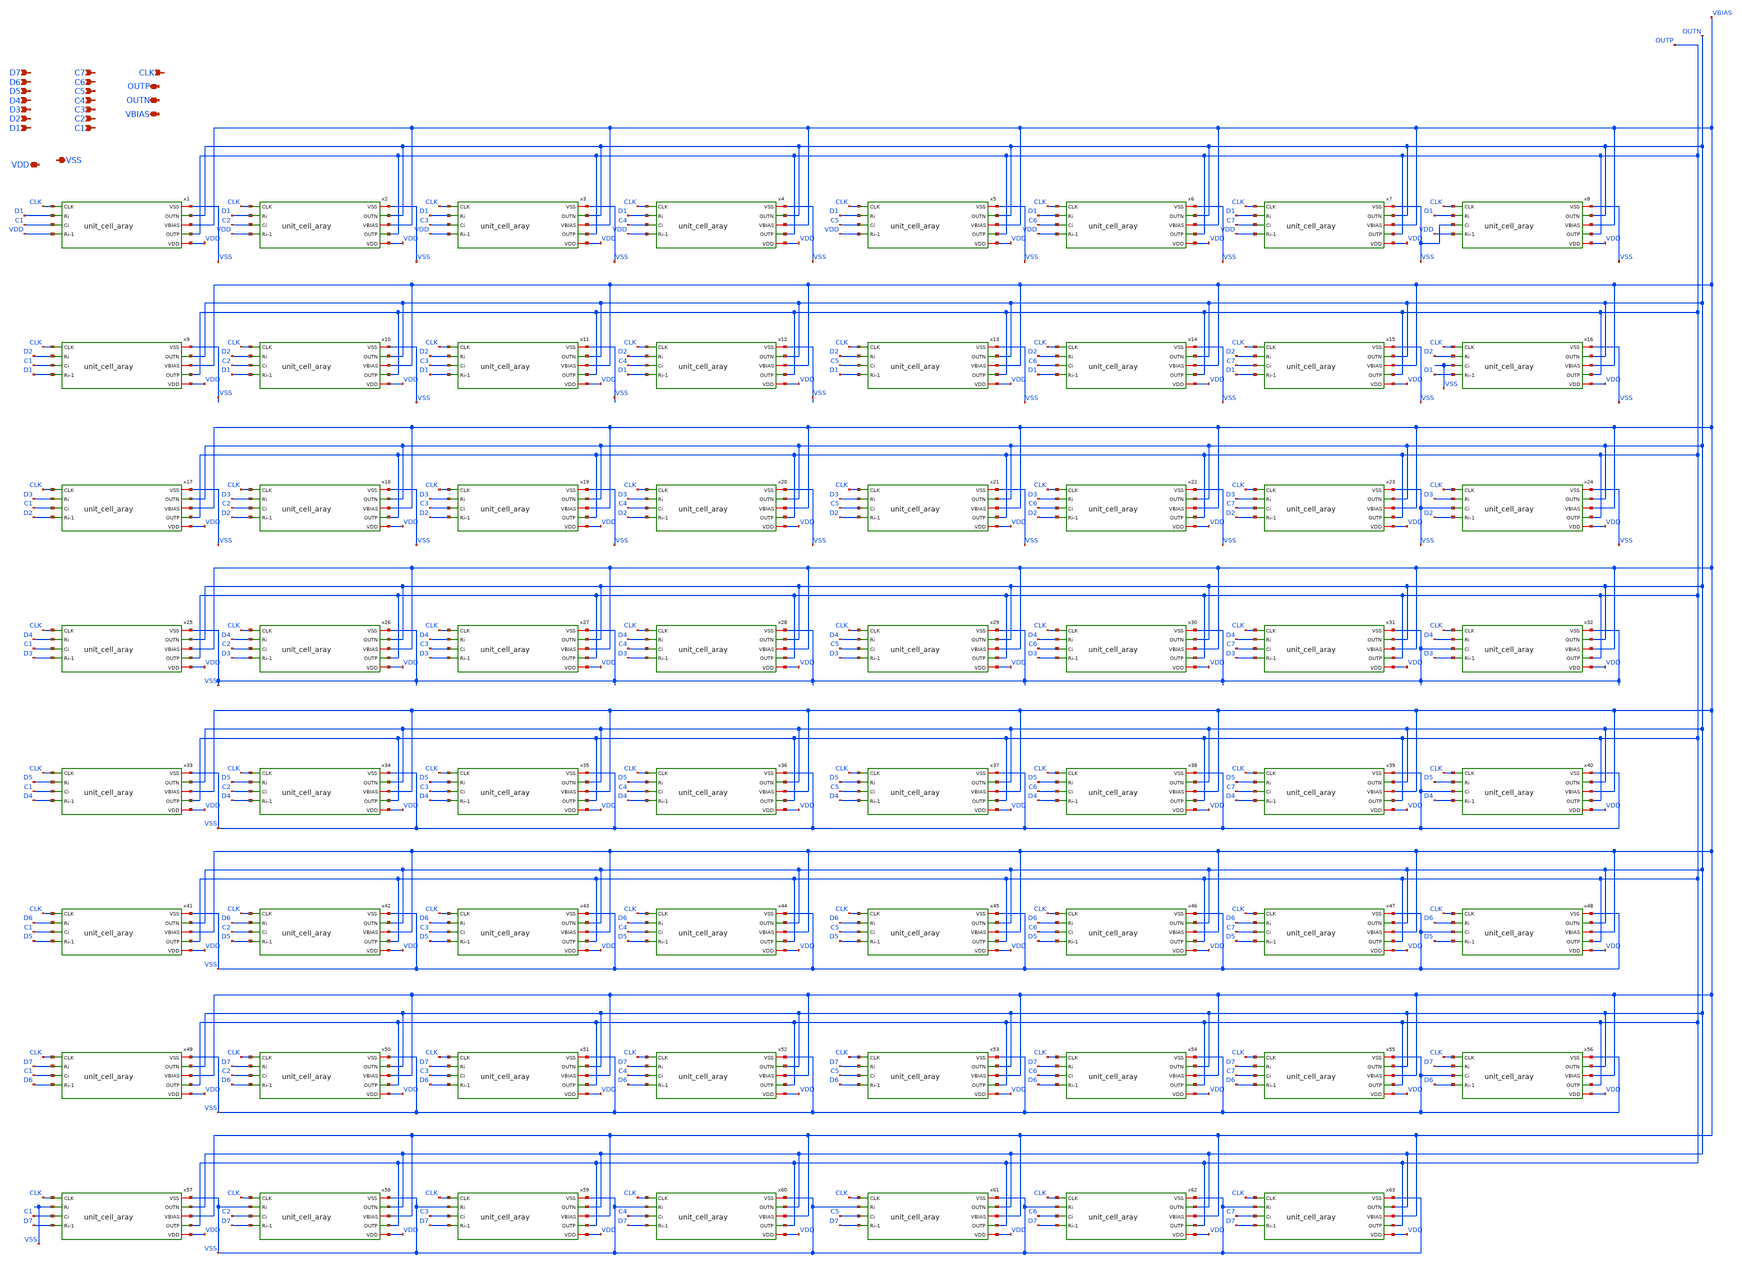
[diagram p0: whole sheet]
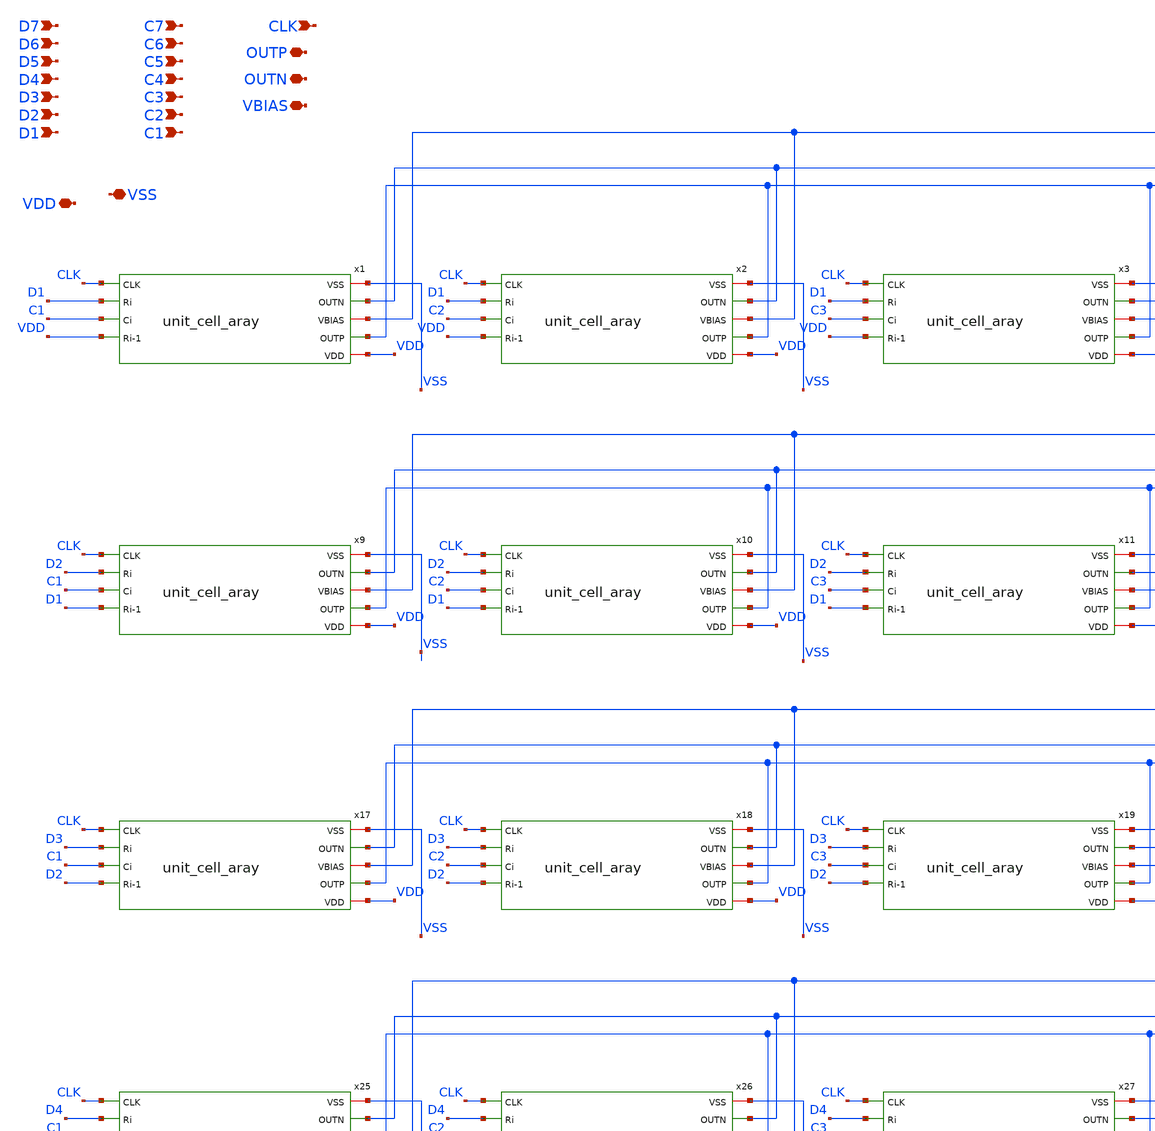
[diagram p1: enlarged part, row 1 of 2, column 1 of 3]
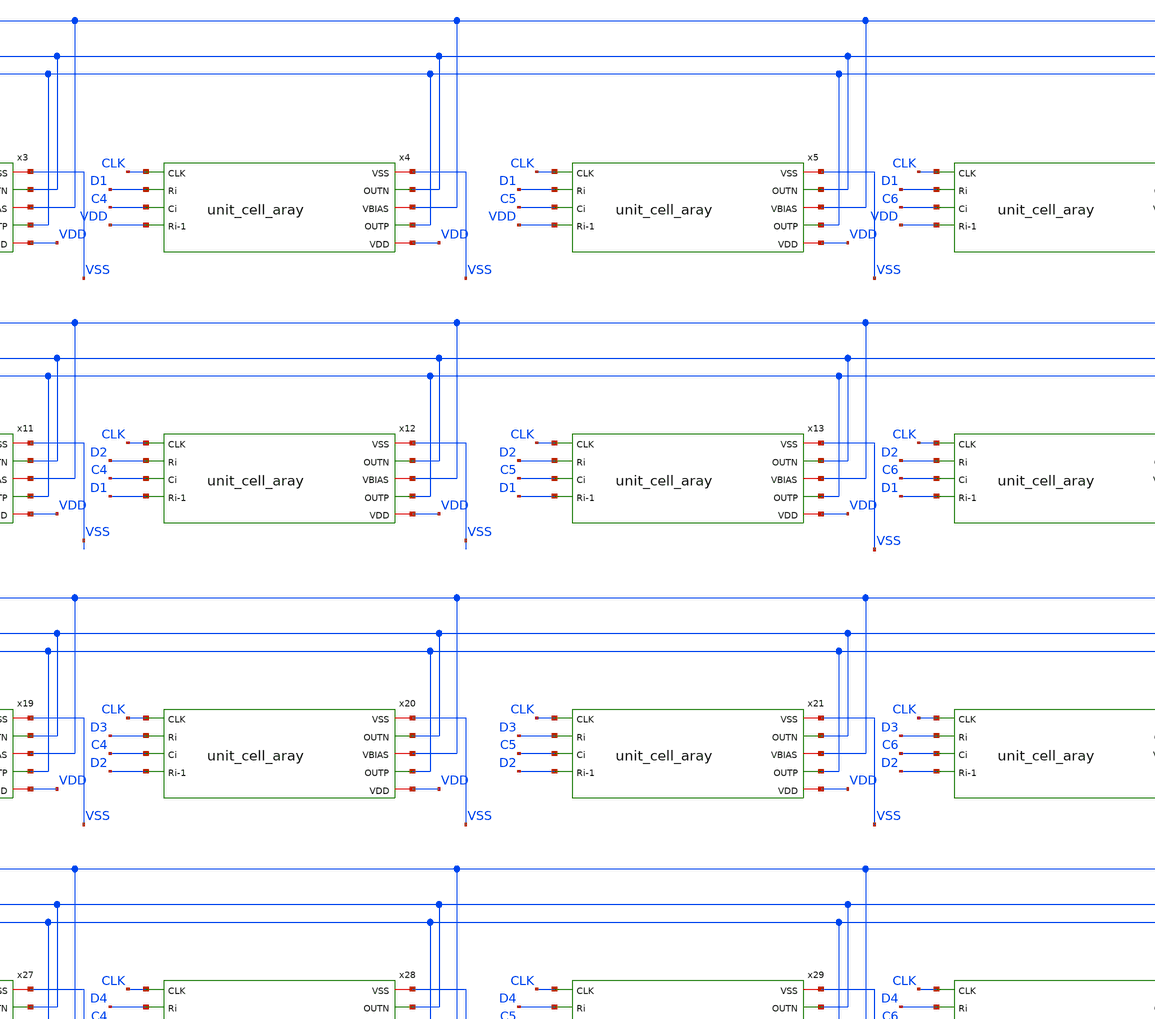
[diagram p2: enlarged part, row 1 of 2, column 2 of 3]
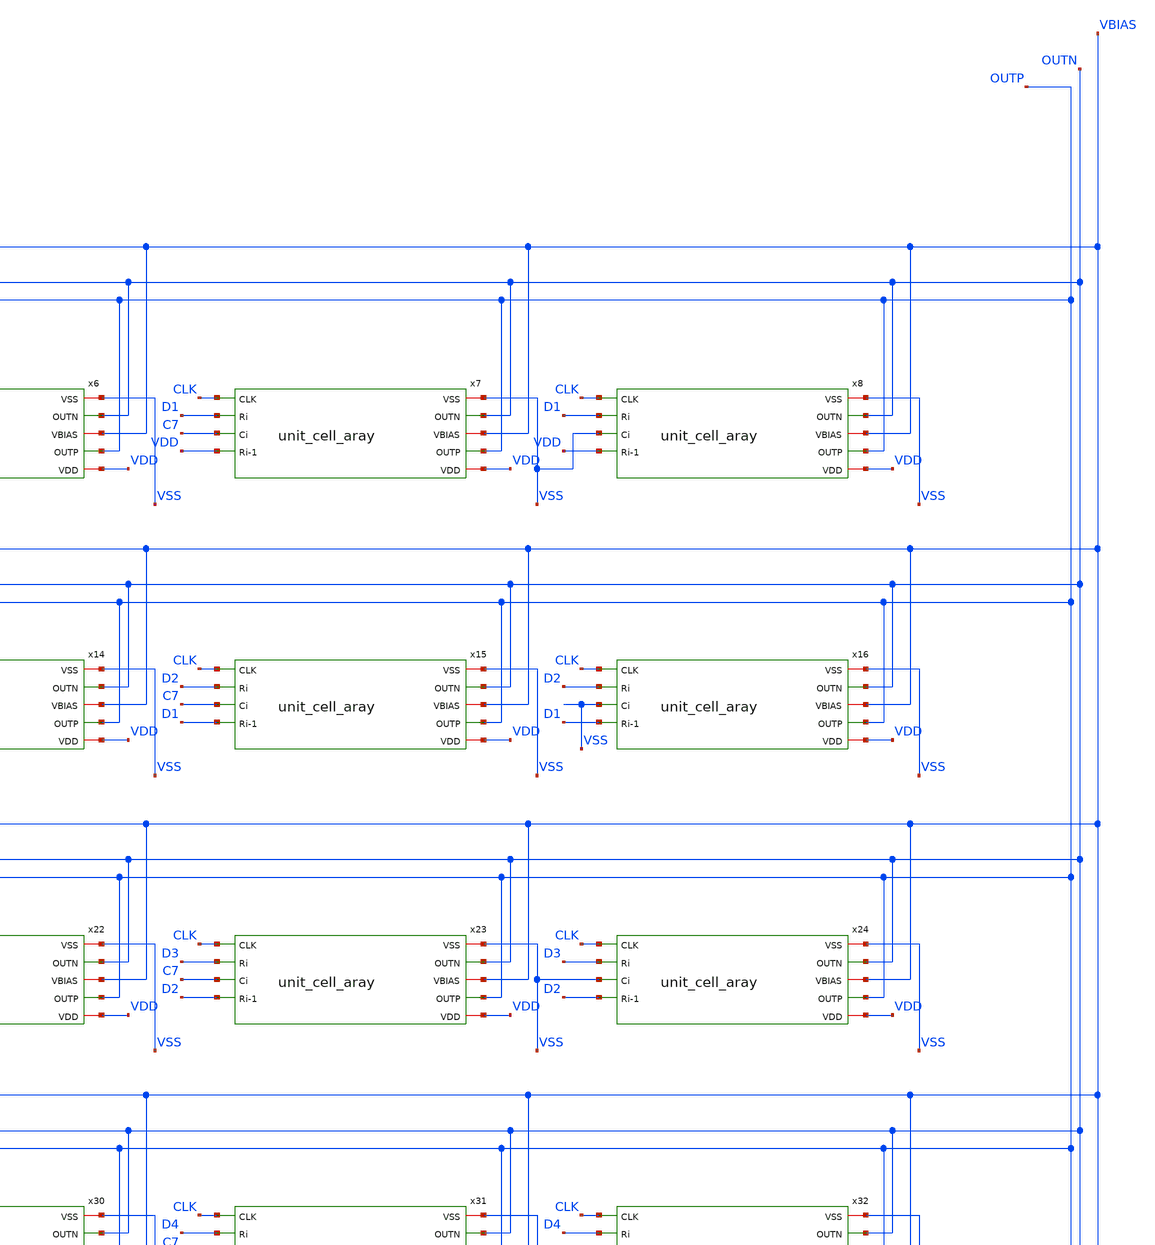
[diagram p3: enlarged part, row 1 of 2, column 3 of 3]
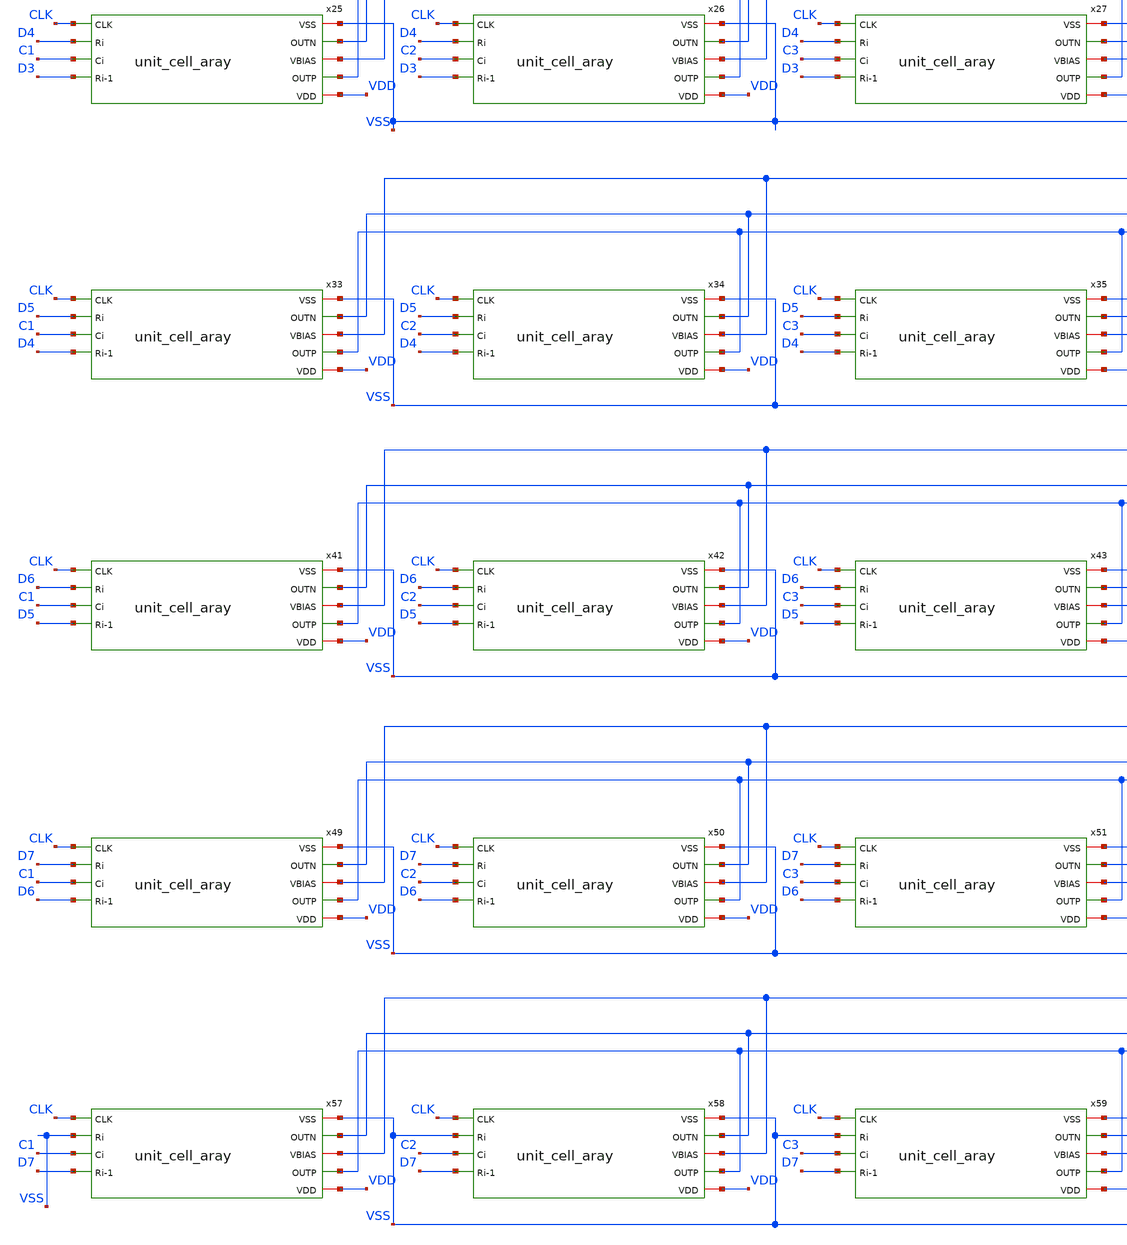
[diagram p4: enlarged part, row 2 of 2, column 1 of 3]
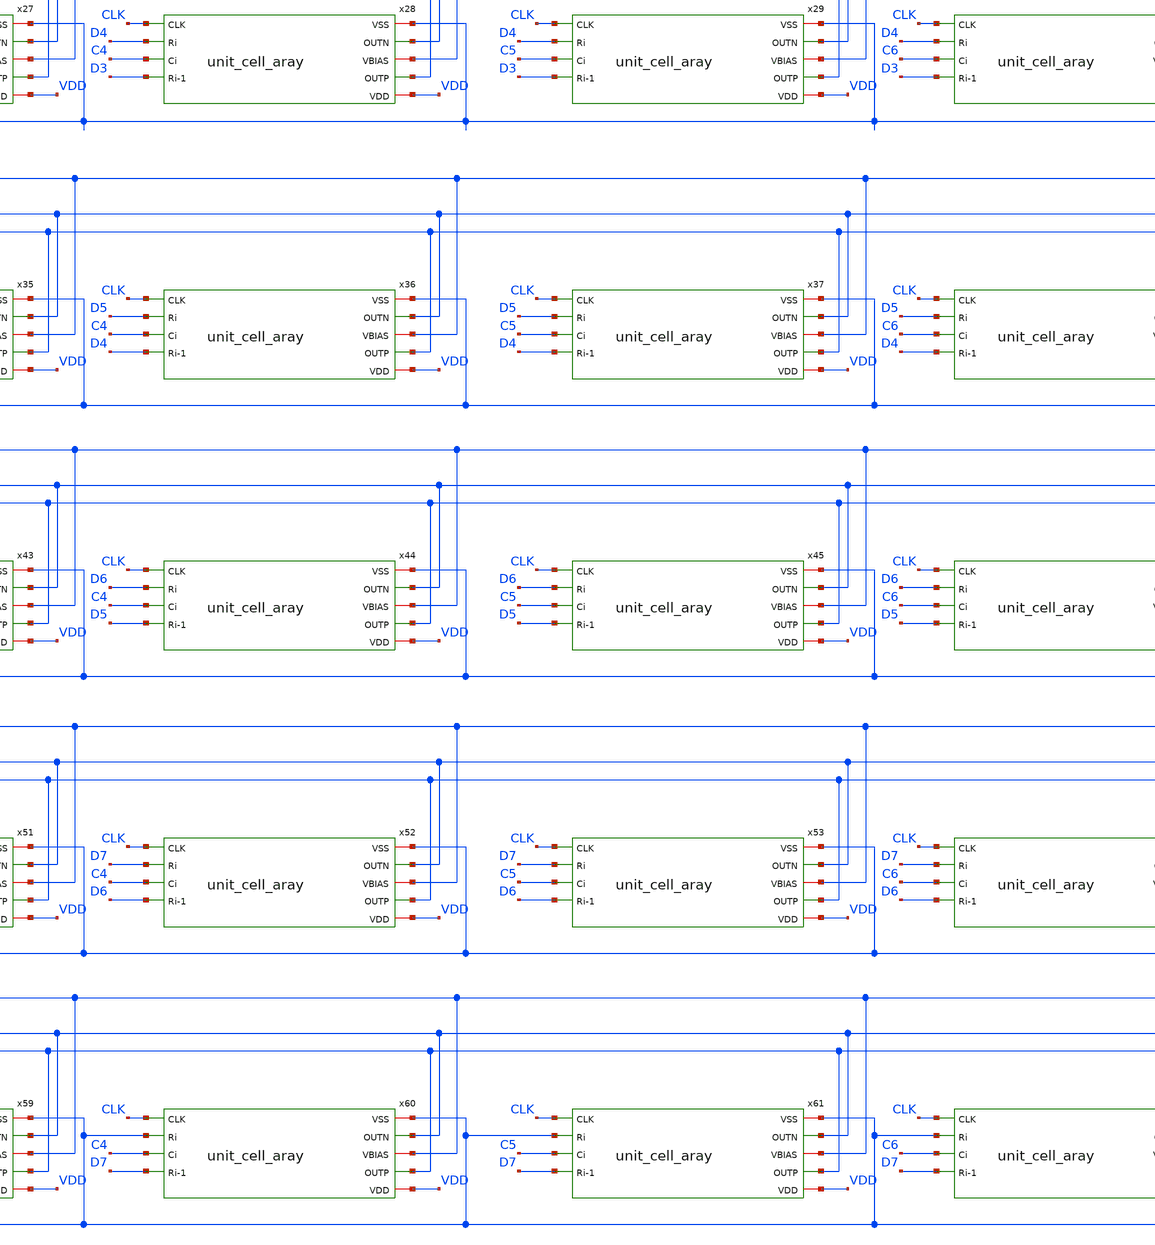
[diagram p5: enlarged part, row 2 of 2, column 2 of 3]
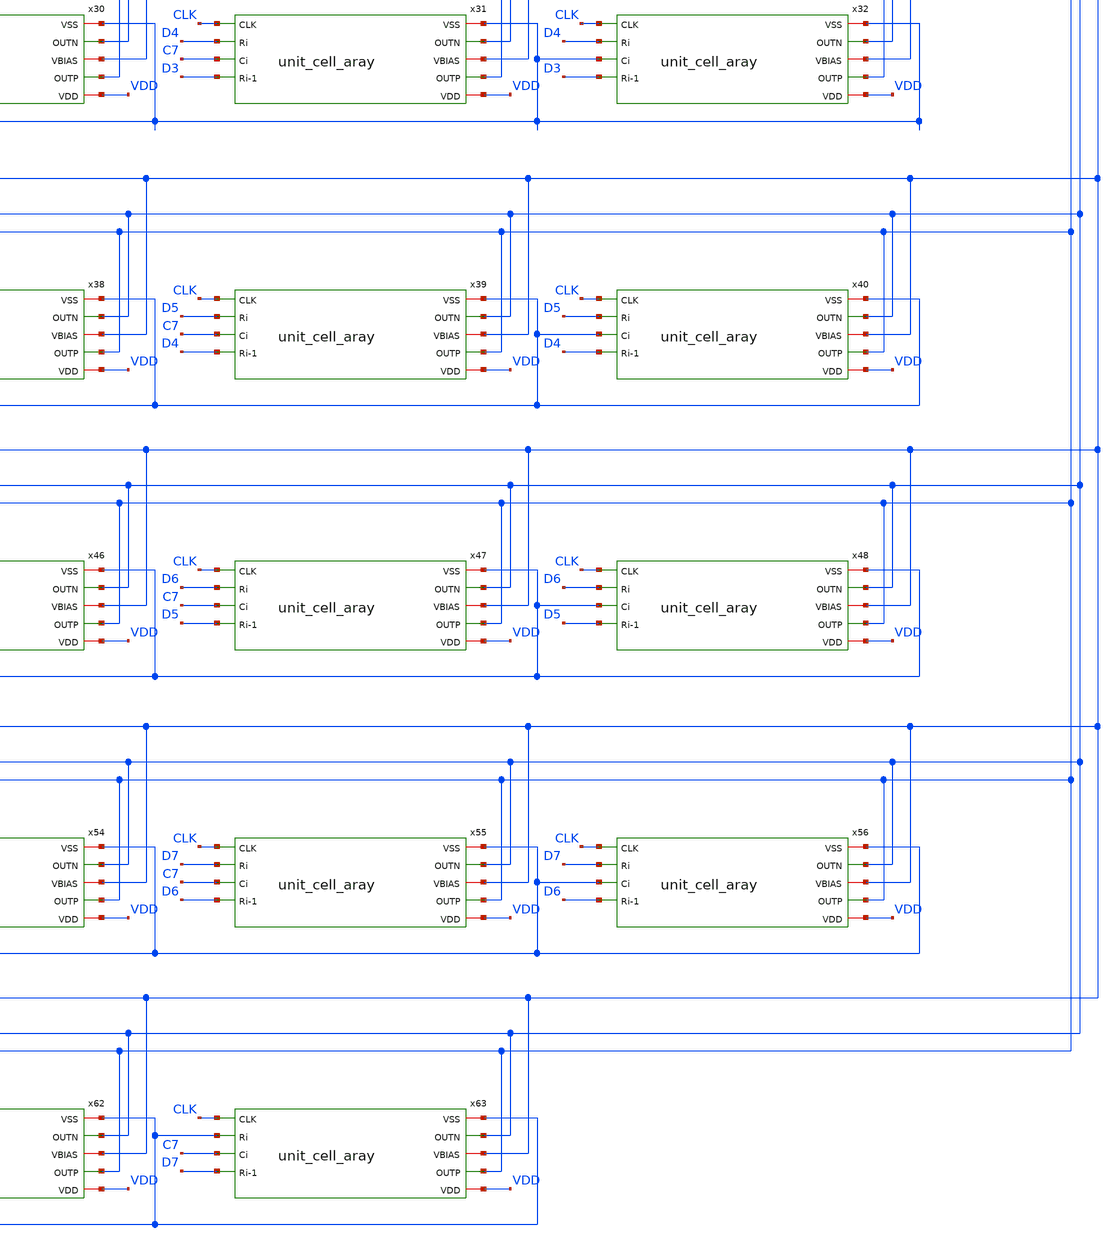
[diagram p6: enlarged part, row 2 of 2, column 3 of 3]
** sch_path: xschem/x6MSB_MATRIX.sch
**.subckt x6MSB_MATRIX D1 D2 D3 D4 D5 D6 D7 C1 C2 C3 C4 C5 C6 C7 CLK OUTP OUTN VBIAS VDD VSS
*.ipin D1
*.ipin D2
*.ipin D3
*.ipin D4
*.ipin D5
*.ipin D6
*.ipin D7
*.ipin C1
*.ipin C2
*.ipin C3
*.ipin C4
*.ipin C5
*.ipin C6
*.ipin C7
*.ipin CLK
*.iopin OUTP
*.iopin OUTN
*.iopin VBIAS
*.iopin VDD
*.iopin VSS
x7 C7 CLK OUTN VBIAS VDD D1 VDD VSS OUTP unit_cell_aray
x8 VSS CLK OUTN VBIAS VDD D1 VDD VSS OUTP unit_cell_aray
x9 C1 CLK OUTN VBIAS D1 D2 VDD VSS OUTP unit_cell_aray
x10 C2 CLK OUTN VBIAS D1 D2 VDD VSS OUTP unit_cell_aray
x11 C3 CLK OUTN VBIAS D1 D2 VDD VSS OUTP unit_cell_aray
x12 C4 CLK OUTN VBIAS D1 D2 VDD VSS OUTP unit_cell_aray
x13 C5 CLK OUTN VBIAS D1 D2 VDD VSS OUTP unit_cell_aray
x14 C6 CLK OUTN VBIAS D1 D2 VDD VSS OUTP unit_cell_aray
x15 C7 CLK OUTN VBIAS D1 D2 VDD VSS OUTP unit_cell_aray
x16 VSS CLK OUTN VBIAS D1 D2 VDD VSS OUTP unit_cell_aray
x17 C1 CLK OUTN VBIAS D2 D3 VDD VSS OUTP unit_cell_aray
x18 C2 CLK OUTN VBIAS D2 D3 VDD VSS OUTP unit_cell_aray
x19 C3 CLK OUTN VBIAS D2 D3 VDD VSS OUTP unit_cell_aray
x20 C4 CLK OUTN VBIAS D2 D3 VDD VSS OUTP unit_cell_aray
x21 C5 CLK OUTN VBIAS D2 D3 VDD VSS OUTP unit_cell_aray
x22 C6 CLK OUTN VBIAS D2 D3 VDD VSS OUTP unit_cell_aray
x23 C7 CLK OUTN VBIAS D2 D3 VDD VSS OUTP unit_cell_aray
x24 VSS CLK OUTN VBIAS D2 D3 VDD VSS OUTP unit_cell_aray
x25 C1 CLK OUTN VBIAS D3 D4 VDD VSS OUTP unit_cell_aray
x26 C2 CLK OUTN VBIAS D3 D4 VDD VSS OUTP unit_cell_aray
x27 C3 CLK OUTN VBIAS D3 D4 VDD VSS OUTP unit_cell_aray
x28 C4 CLK OUTN VBIAS D3 D4 VDD VSS OUTP unit_cell_aray
x29 C5 CLK OUTN VBIAS D3 D4 VDD VSS OUTP unit_cell_aray
x30 C6 CLK OUTN VBIAS D3 D4 VDD VSS OUTP unit_cell_aray
x31 C7 CLK OUTN VBIAS D3 D4 VDD VSS OUTP unit_cell_aray
x32 VSS CLK OUTN VBIAS D3 D4 VDD VSS OUTP unit_cell_aray
x33 C1 CLK OUTN VBIAS D4 D5 VDD VSS OUTP unit_cell_aray
x34 C2 CLK OUTN VBIAS D4 D5 VDD VSS OUTP unit_cell_aray
x35 C3 CLK OUTN VBIAS D4 D5 VDD VSS OUTP unit_cell_aray
x36 C4 CLK OUTN VBIAS D4 D5 VDD VSS OUTP unit_cell_aray
x37 C5 CLK OUTN VBIAS D4 D5 VDD VSS OUTP unit_cell_aray
x38 C6 CLK OUTN VBIAS D4 D5 VDD VSS OUTP unit_cell_aray
x39 C7 CLK OUTN VBIAS D4 D5 VDD VSS OUTP unit_cell_aray
x40 VSS CLK OUTN VBIAS D4 D5 VDD VSS OUTP unit_cell_aray
x41 C1 CLK OUTN VBIAS D5 D6 VDD VSS OUTP unit_cell_aray
x42 C2 CLK OUTN VBIAS D5 D6 VDD VSS OUTP unit_cell_aray
x43 C3 CLK OUTN VBIAS D5 D6 VDD VSS OUTP unit_cell_aray
x44 C4 CLK OUTN VBIAS D5 D6 VDD VSS OUTP unit_cell_aray
x45 C5 CLK OUTN VBIAS D5 D6 VDD VSS OUTP unit_cell_aray
x46 C6 CLK OUTN VBIAS D5 D6 VDD VSS OUTP unit_cell_aray
x47 C7 CLK OUTN VBIAS D5 D6 VDD VSS OUTP unit_cell_aray
x48 VSS CLK OUTN VBIAS D5 D6 VDD VSS OUTP unit_cell_aray
x49 C1 CLK OUTN VBIAS D6 D7 VDD VSS OUTP unit_cell_aray
x50 C2 CLK OUTN VBIAS D6 D7 VDD VSS OUTP unit_cell_aray
x51 C3 CLK OUTN VBIAS D6 D7 VDD VSS OUTP unit_cell_aray
x52 C4 CLK OUTN VBIAS D6 D7 VDD VSS OUTP unit_cell_aray
x53 C5 CLK OUTN VBIAS D6 D7 VDD VSS OUTP unit_cell_aray
x54 C6 CLK OUTN VBIAS D6 D7 VDD VSS OUTP unit_cell_aray
x55 C7 CLK OUTN VBIAS D6 D7 VDD VSS OUTP unit_cell_aray
x56 VSS CLK OUTN VBIAS D6 D7 VDD VSS OUTP unit_cell_aray
x57 C1 CLK OUTN VBIAS D7 VSS VDD VSS OUTP unit_cell_aray
x58 C2 CLK OUTN VBIAS D7 VSS VDD VSS OUTP unit_cell_aray
x59 C3 CLK OUTN VBIAS D7 VSS VDD VSS OUTP unit_cell_aray
x60 C4 CLK OUTN VBIAS D7 VSS VDD VSS OUTP unit_cell_aray
x61 C5 CLK OUTN VBIAS D7 VSS VDD VSS OUTP unit_cell_aray
x62 C6 CLK OUTN VBIAS D7 VSS VDD VSS OUTP unit_cell_aray
x63 C7 CLK OUTN VBIAS D7 VSS VDD VSS OUTP unit_cell_aray
x1 C1 CLK OUTN VBIAS VDD D1 VDD VSS OUTP unit_cell_aray
x2 C2 CLK OUTN VBIAS VDD D1 VDD VSS OUTP unit_cell_aray
x3 C3 CLK OUTN VBIAS VDD D1 VDD VSS OUTP unit_cell_aray
x4 C4 CLK OUTN VBIAS VDD D1 VDD VSS OUTP unit_cell_aray
x5 C5 CLK OUTN VBIAS VDD D1 VDD VSS OUTP unit_cell_aray
x6 C6 CLK OUTN VBIAS VDD D1 VDD VSS OUTP unit_cell_aray
**.ends
.end
